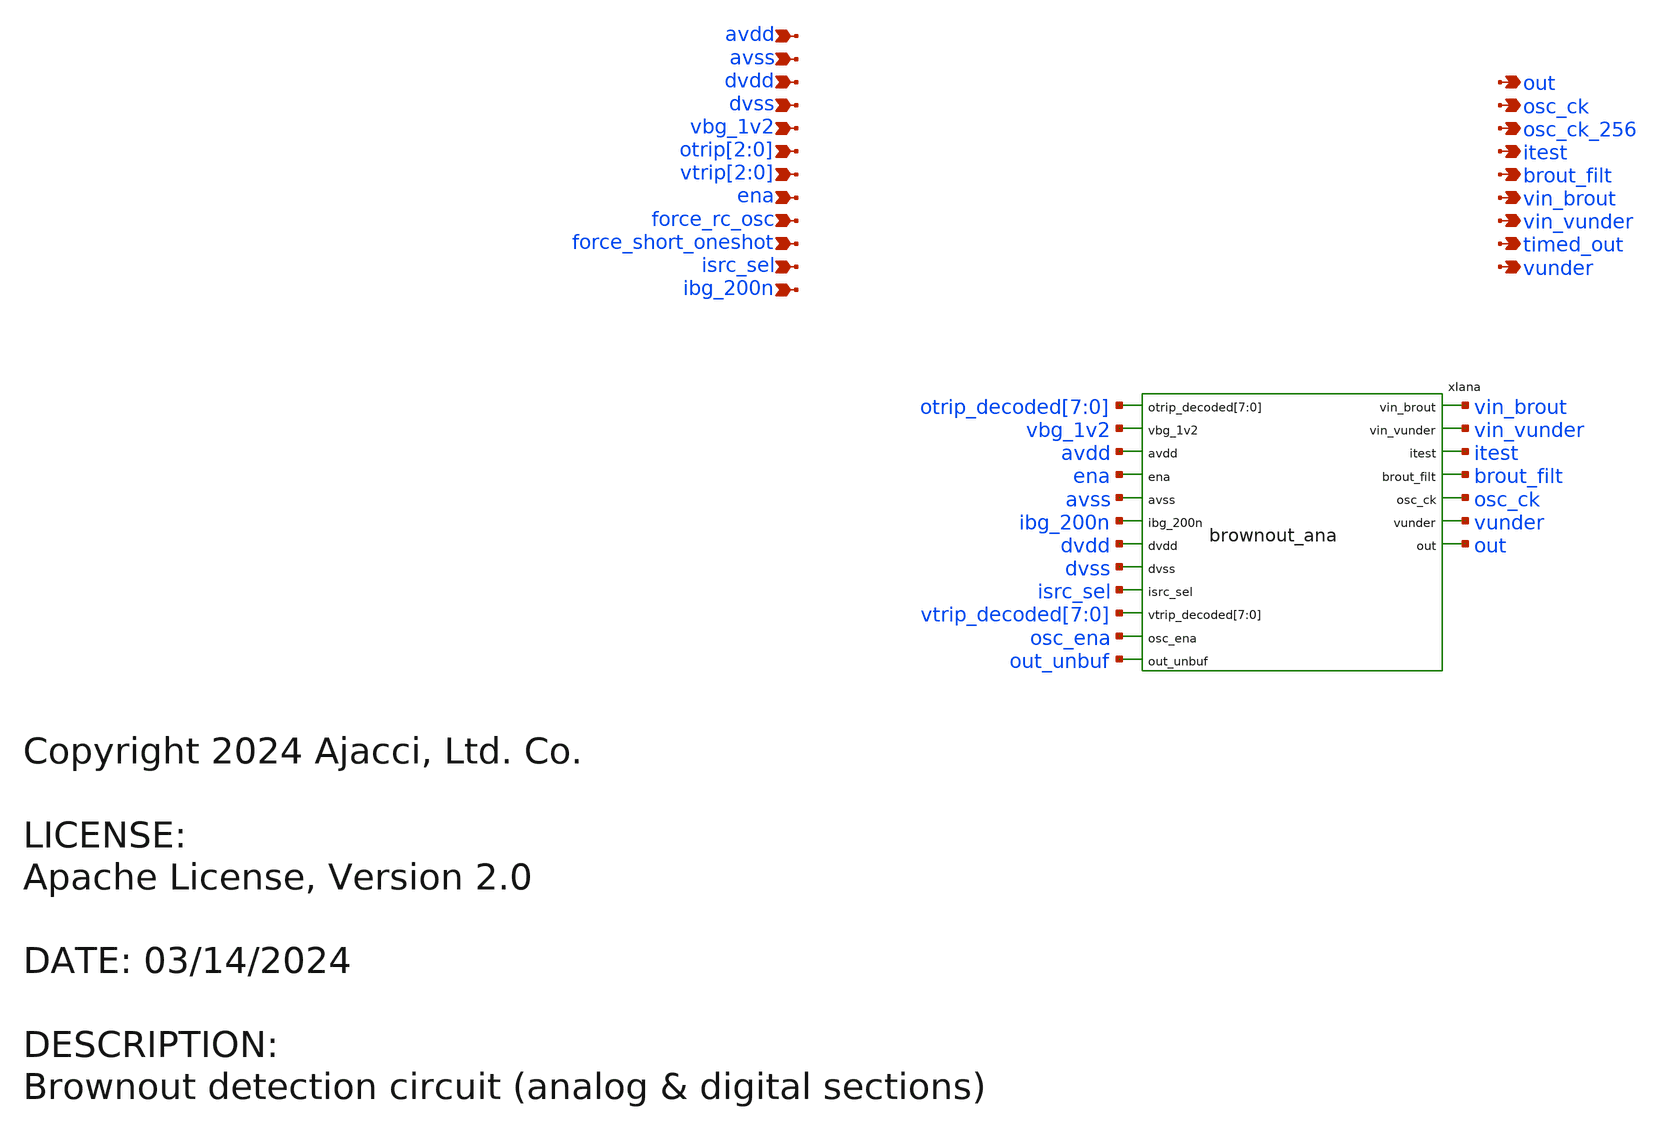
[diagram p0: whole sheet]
** sch_path: xschem/brownout.sch
* Copyright 2024 Ajacci, Ltd. Co.
* LICENSE:
* Apache License, Version 2.0
**.subckt brownout avdd avss dvdd dvss vbg_1v2 otrip[2],otrip[1],otrip[0] ena force_rc_osc
*+ force_short_oneshot isrc_sel ibg_200n vin_brout out osc_ck osc_ck_256 brout_filt itest timed_out
*+ vtrip[2],vtrip[1],vtrip[0] vin_vunder vunder
*.ipin avdd
*.ipin avss
*.ipin dvdd
*.ipin dvss
*.ipin vbg_1v2
*.ipin otrip[2],otrip[1],otrip[0]
*.ipin ena
*.ipin force_rc_osc
*.ipin force_short_oneshot
*.ipin isrc_sel
*.ipin ibg_200n
*.opin vin_brout
*.opin out
*.opin osc_ck
*.opin osc_ck_256
*.opin brout_filt
*.opin itest
*.opin timed_out
*.ipin vtrip[2],vtrip[1],vtrip[0]
*.opin vin_vunder
*.opin vunder
xIana vin_brout vin_vunder otrip_decoded[7] otrip_decoded[6] otrip_decoded[5] otrip_decoded[4]
+ otrip_decoded[3] otrip_decoded[2] otrip_decoded[1] otrip_decoded[0] vbg_1v2 avdd itest ena avss ibg_200n dvdd dvss
+ isrc_sel vtrip_decoded[7] vtrip_decoded[6] vtrip_decoded[5] vtrip_decoded[4] vtrip_decoded[3]
+ vtrip_decoded[2] vtrip_decoded[1] vtrip_decoded[0] brout_filt osc_ck osc_ena vunder out out_unbuf brownout_ana
**** begin user architecture code



*XSPICE CO-SIM netlist
.include brownout_dig.out.spice
xibrownout_dig dvss dvdd brout_filt ena force_rc_osc force_short_oneshot osc_ck osc_ck_256 osc_ena
+  otrip_0_ otrip_1_ otrip_2_ otrip_decoded_0_ otrip_decoded_1_ otrip_decoded_2_ otrip_decoded_3_
+ otrip_decoded_4_ otrip_decoded_5_ otrip_decoded_6_ otrip_decoded_7_ out_unbuf timed_out vtrip_0_ vtrip_1_ vtrip_2_
+ vtrip_decoded_0_ vtrip_decoded_1_ vtrip_decoded_2_ vtrip_decoded_3_ vtrip_decoded_4_ vtrip_decoded_5_
+ vtrip_decoded_6_ vtrip_decoded_7_ brownout_dig


**** end user architecture code
**.ends
.end
